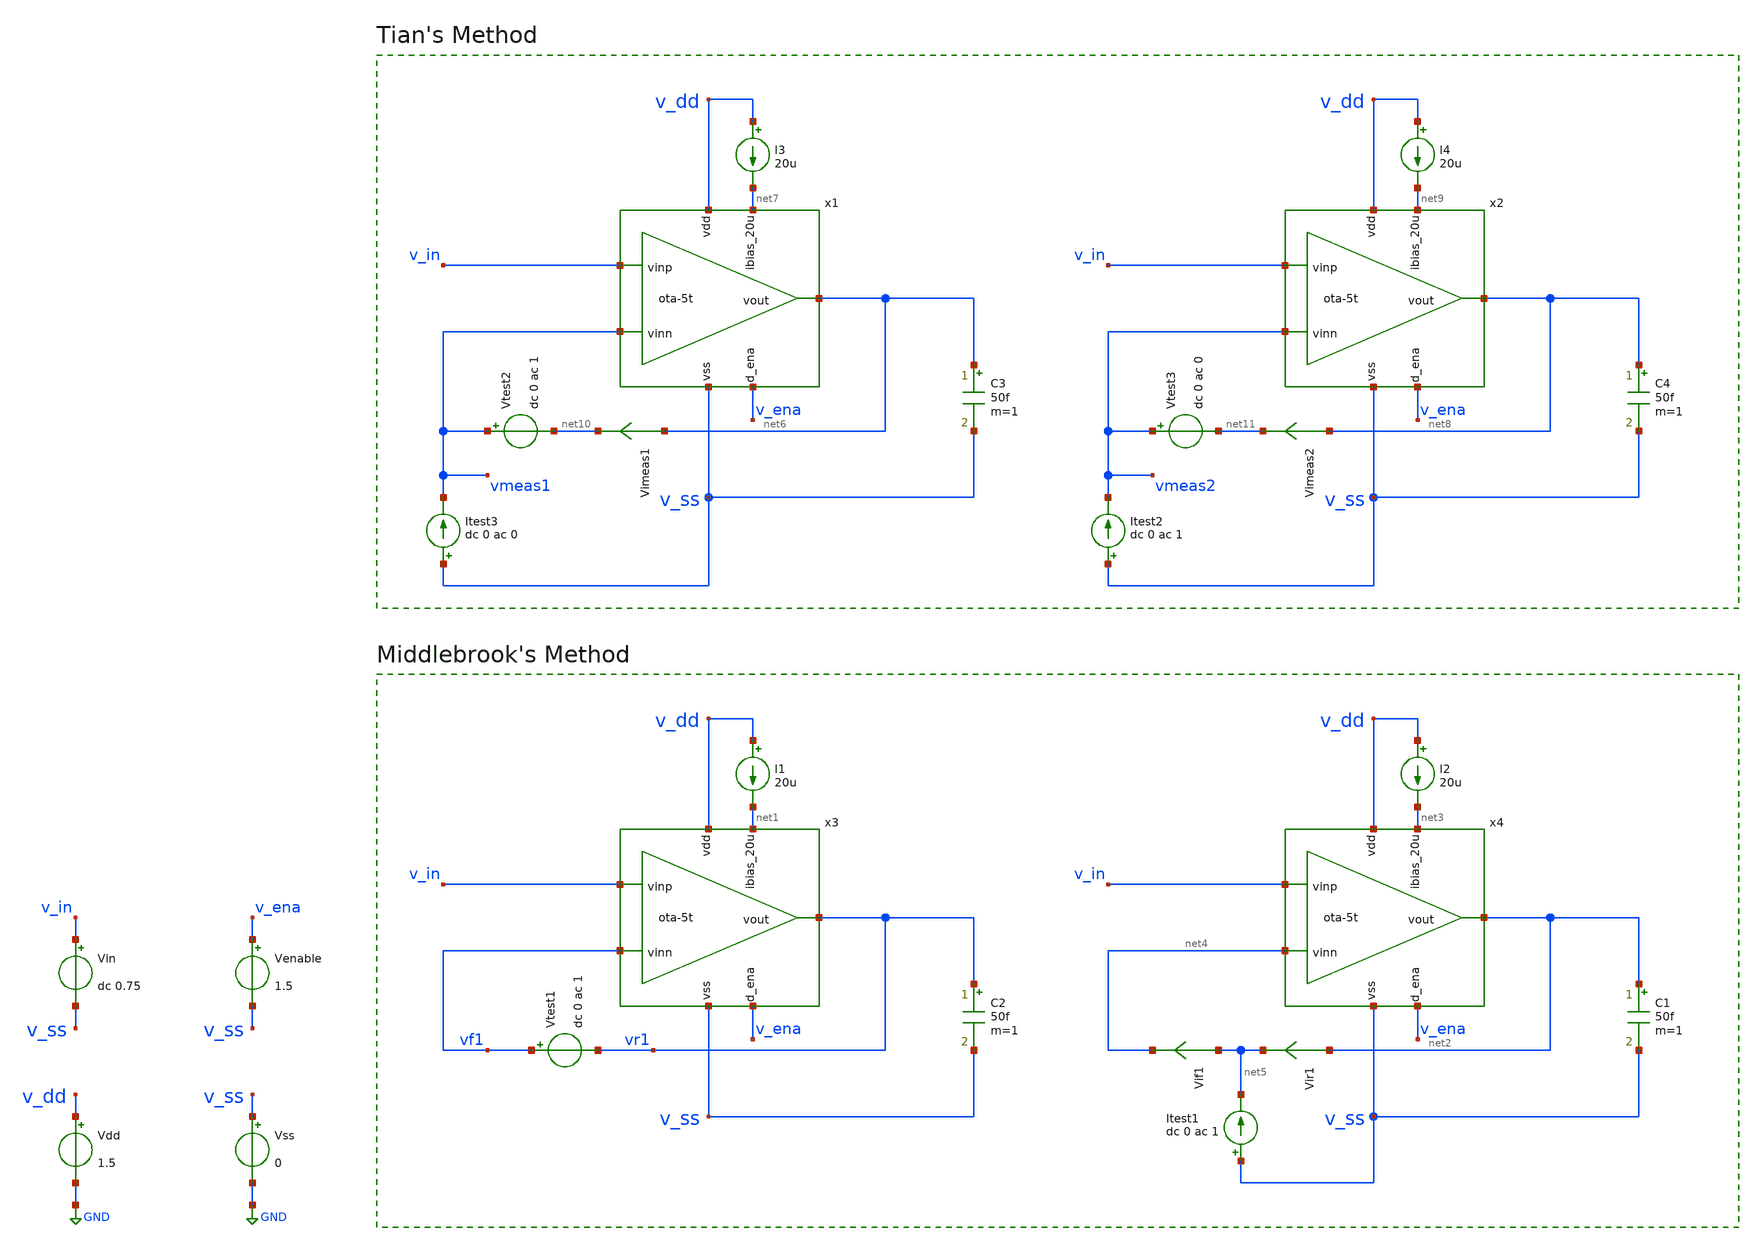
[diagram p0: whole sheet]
** sch_path: 004_Real_Circuits/001_version_basic_ota_pretl/ota-5t_tb-loopgain..sch
* (c) 2024-2025 H. Pretl, S. Dorrer, Apache-2.0 license
* 004_Real_Circuits/001_version_basic_ota_pretl/ota-5t.sch:
* (c) 2024-2025 Harald Pretl, Apache-2.0 license
**.subckt ota-5t_tb-loopgain.
Vdd v_dd GND 1.5
Vss v_ss GND 0
Vin v_in v_ss dc 0.75
Venable v_ena v_ss 1.5
C2 vr1 v_ss 50f m=1
I1 v_dd net1 20u
Vtest1 vf1 vr1 dc 0 ac 1
C1 net2 v_ss 50f m=1
I2 v_dd net3 20u
Vir1 net2 net5 0
.save i(vir1)
Vif1 net5 net4 0
.save i(vif1)
Itest1 v_ss net5 dc 0 ac 1
C3 net6 v_ss 50f m=1
I3 v_dd net7 20u
C4 net8 v_ss 50f m=1
I4 v_dd net9 20u
Itest3 v_ss vmeas1 dc 0 ac 0
Vtest2 vmeas1 net10 dc 0 ac 1
Vimeas1 net6 net10 0
.save i(vimeas1)
Itest2 v_ss vmeas2 dc 0 ac 1
Vtest3 vmeas2 net11 dc 0 ac 0
Vimeas2 net8 net11 0
.save i(vimeas2)
x1 v_dd net6 v_in vmeas1 net7 v_ena v_ss ota-5t
x2 v_dd net8 v_in vmeas2 net9 v_ena v_ss ota-5t
x4 v_dd net2 v_in net4 net3 v_ena v_ss ota-5t
x3 v_dd vr1 v_in vf1 net1 v_ena v_ss ota-5t
**** begin user architecture code
 .lib cornerMOSlv.lib mos_tt



.param temp=27
.options savecurrents reltol=1e-3 abstol=1e-12 gmin=1e-15
.control
save all

* Operating Point Analysis
op
remzerovec
write ota-5t_tb-loopgain.raw
set appendwrite

* AC Analysis
ac dec 101 1 100G
remzerovec
write ota-5t_tb-loopgain.raw
set appendwrite

* Middlebrook's Method
let tv=-v(vr1)/v(vf1)
let ti=-i(vir1)/i(vif1)
let tmb=(tv*ti - 1)/(tv + ti + 2)

plot db(tmb) ylabel 'Magnitude - Middlebrook'
plot 180/pi*cphase(tmb) ylabel 'Phase - Middlebrook'

* Tian's Method
* vtest=0, itest=1:
let A=i(Vimeas2)
let C=v(vmeas2)

* vtest=1, itest=0:
let B=i(Vimeas1)
let D=v(vmeas1)
let ttian=(A*D-B*C-A)/(2*(B*C-A*D)+A-D+1)

plot db(ttian) ylabel 'Magnitude - Tian'
plot 180/pi*cphase(ttian) ylabel 'Phase - Tian'

* Middlebrook vs. Tian
plot db(tmb) db(ttian) ylabel 'Magnitude'
plot 180/pi*cphase(tmb) 180/pi*cphase(ttian) ylabel 'Phase'

write ota-5t_tb-loopgain.raw

*quit
.endc


**** end user architecture code
**.ends

* expanding   symbol:  004_Real_Circuits/001_version_basic_ota_pretl/ota-5t.sym # of pins=7
** sym_path: 004_Real_Circuits/001_version_basic_ota_pretl/ota-5t.sym
** sch_path: 004_Real_Circuits/001_version_basic_ota_pretl/ota-5t.sch
.subckt ota-5t vdd vout vinp vinn ibias_20u d_ena vss
*.ipin ibias_20u
*.iopin vdd
*.iopin vss
*.ipin vinp
*.ipin vinn
*.opin vout
*.ipin d_ena
XM5 tail gate_n vss vss sg13_lv_nmos w=1.5u l=5u ng=1 m=1 mm_ok=1
XM4 vout gate_p vdd vdd sg13_lv_pmos w=3.5u l=5u ng=1 m=1 mm_ok=1
XM1 gate_p vinp tail vss sg13_lv_nmos w=2u l=5u ng=1 m=1 mm_ok=1
XM2 vout vinn tail vss sg13_lv_nmos w=2u l=5u ng=1 m=1 mm_ok=1
XM3 gate_p gate_p vdd vdd sg13_lv_pmos w=3.5u l=5u ng=1 m=1 mm_ok=1
XM6 ibias_20u gate_n vss vss sg13_lv_nmos w=10u l=5u ng=5 m=1 mm_ok=1
XM9 gate_n ena_n vss vss sg13_lv_nmos w=0.5u l=0.13u ng=1 m=1 mm_ok=1
XM11 gate_p ena vdd vdd sg13_lv_pmos w=1.5u l=0.13u ng=1 m=1 mm_ok=1
XM7 ena ena_n vss vss sg13_lv_nmos w=0.5u l=0.13u ng=1 m=1 mm_ok=1
XM8 ena ena_n vdd vdd sg13_lv_pmos w=1.5u l=0.13u ng=1 m=1 mm_ok=1
XM10 ibias_20u ena gate_n vss sg13_lv_nmos w=0.5u l=0.13u ng=1 m=1 mm_ok=1
XM12 ena_n d_ena vss vss sg13_lv_nmos w=0.5u l=0.13u ng=1 m=1 mm_ok=1
XM13 ena_n d_ena vdd vdd sg13_lv_pmos w=1.5u l=0.13u ng=1 m=1 mm_ok=1
.ends

.GLOBAL GND
.end
